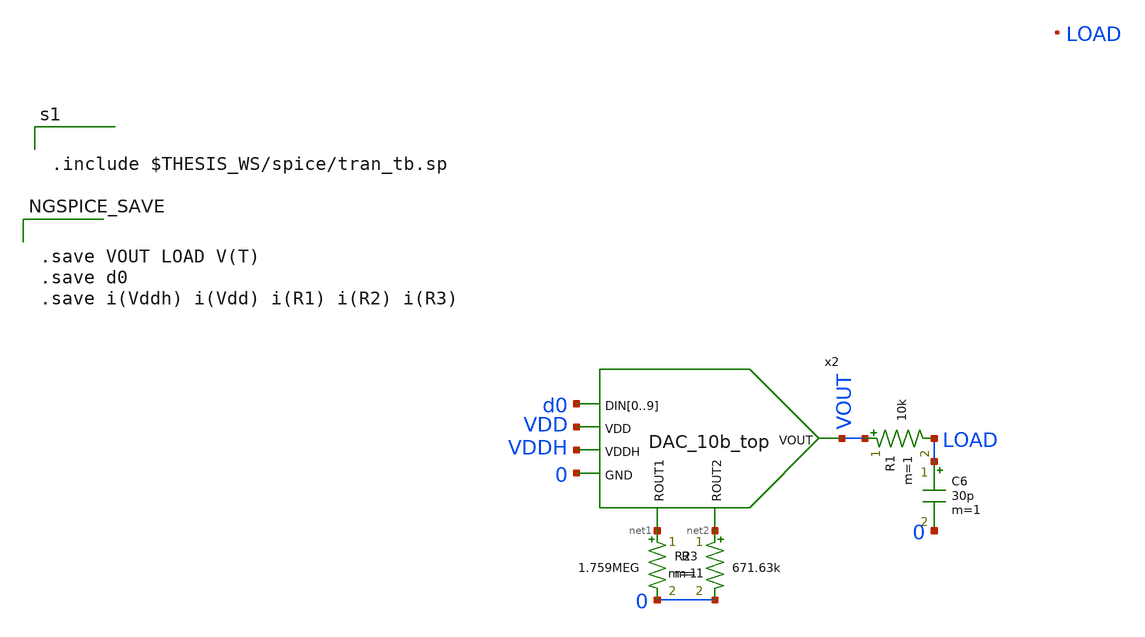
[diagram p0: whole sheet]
** sch_path: xschem/10b_DAC_tran-tb.sch
.lib $::SKYWATER_MODELS/sky130.lib.spice tt
.include $::SKYWATER_STDCELLS/sky130_fd_sc_hd.spice
.include ~/pdk/sky130A/libs.ref/sky130_fd_sc_hvl/spice/sky130_fd_sc_hvl.spice

**.subckt 10b_DAC_tran-tb
C6 LOAD 0 30p m=1
R1 VOUT LOAD 10k m=1
R2 net1 0 1.759MEG m=1
R3 net2 0 671.63k m=1
x2 d0 d0 d0 d0 d0 d0 d0 d0 d0 d0 net1 net2 VDD VDDH 0 VOUT DAC_10b_top
**** begin user architecture code


.include $THESIS_WS/spice/tran_tb.sp



.save VOUT LOAD V(T)
.save d0
.save i(Vddh) i(Vdd) i(R1) i(R2) i(R3)


**** end user architecture code
**.ends
.end
